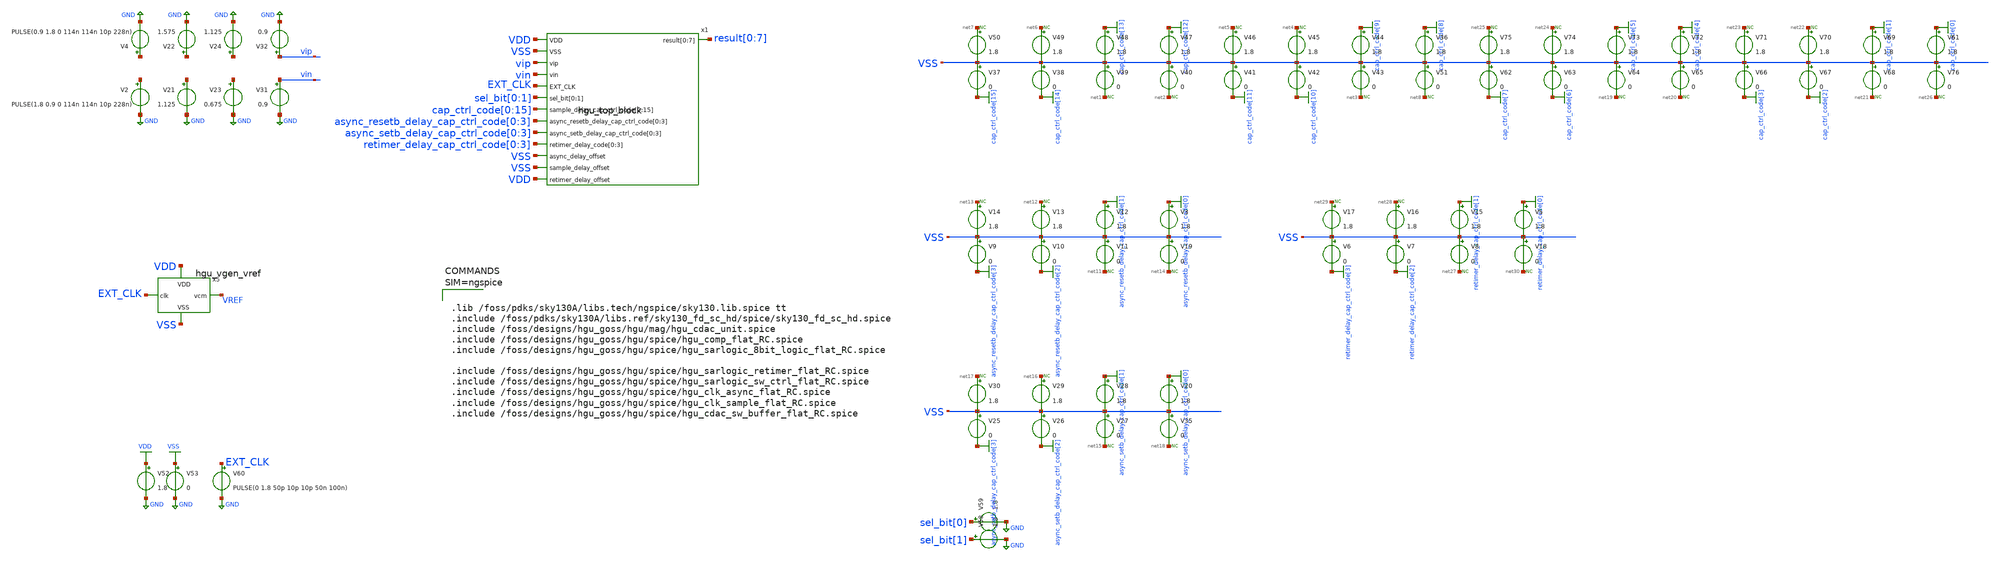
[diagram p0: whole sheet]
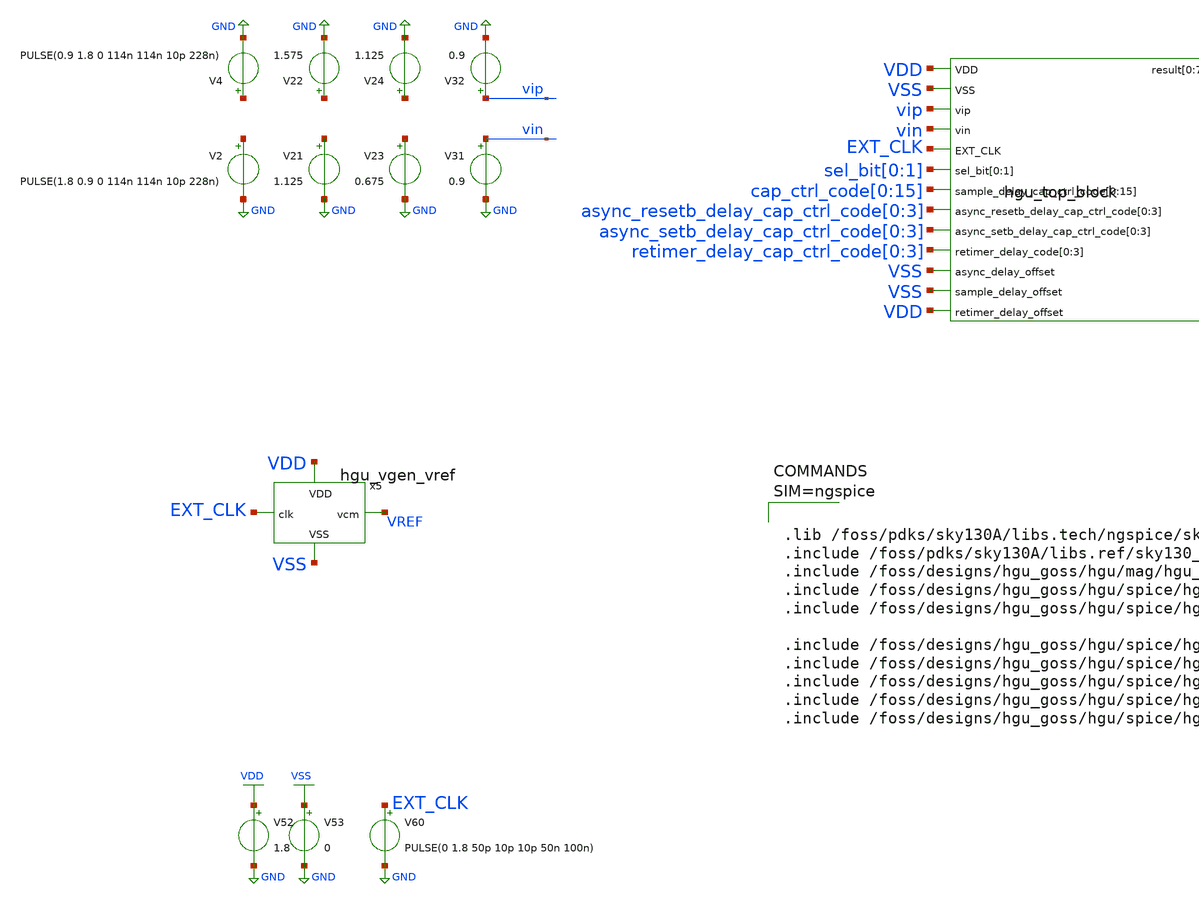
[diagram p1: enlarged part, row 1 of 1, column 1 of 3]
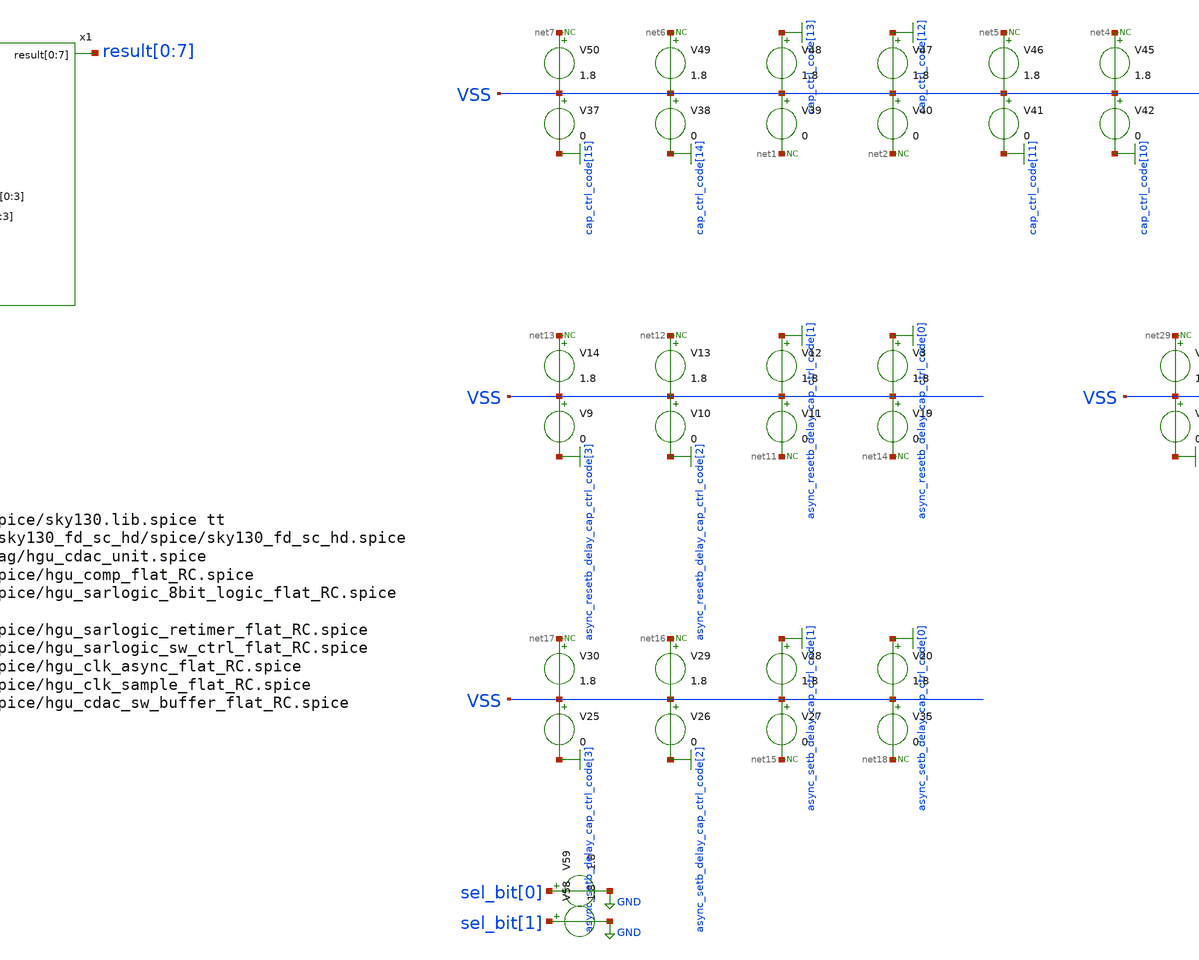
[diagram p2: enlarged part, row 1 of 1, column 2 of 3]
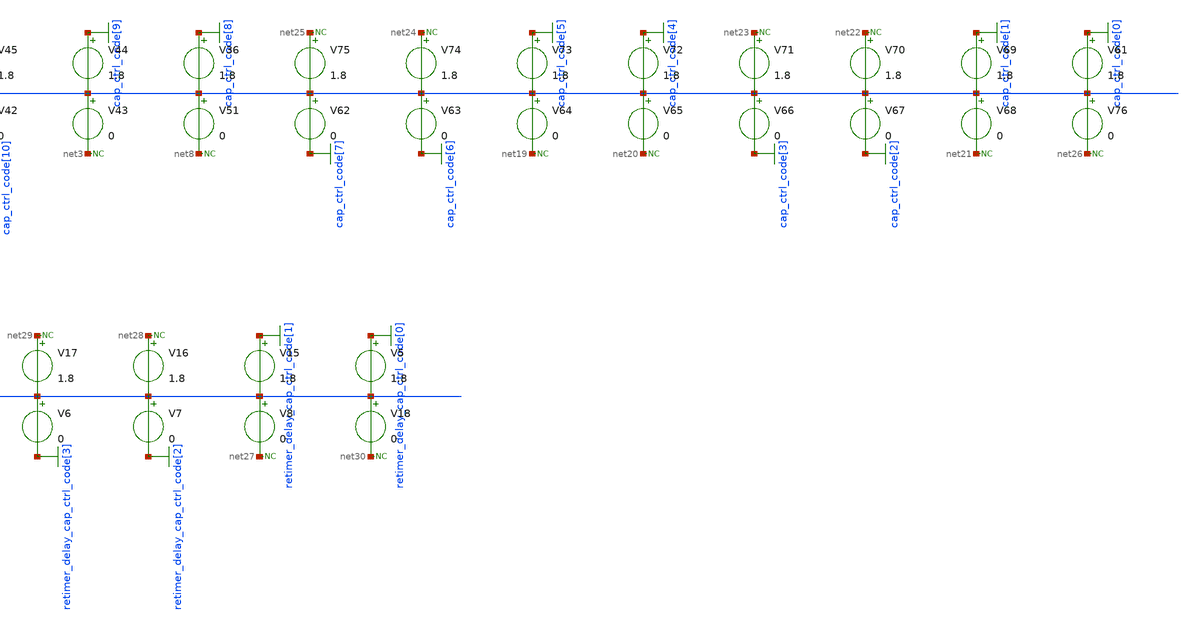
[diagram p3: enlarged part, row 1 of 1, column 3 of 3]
** sch_path: hgu/xschem/untitled-1.sch
**.subckt untitled-1
V36 cap_ctrl_code[8] VSS 1.8
V37 VSS cap_ctrl_code[15] 0
V38 VSS cap_ctrl_code[14] 0
V39 VSS net1 0
V40 VSS net2 0
V41 VSS cap_ctrl_code[11] 0
V42 VSS cap_ctrl_code[10] 0
V43 VSS net3 0
V44 cap_ctrl_code[9] VSS 1.8
V45 net4 VSS 1.8
V46 net5 VSS 1.8
V47 cap_ctrl_code[12] VSS 1.8
V48 cap_ctrl_code[13] VSS 1.8
V49 net6 VSS 1.8
V50 net7 VSS 1.8
V51 VSS net8 0
* noconn #net7
* noconn #net6
* noconn #net1
* noconn #net2
* noconn #net5
* noconn #net4
* noconn #net3
* noconn #net8
V52 VDD GND 1.8
V53 VSS GND 0
V60 EXT_CLK GND PULSE(0 1.8 50p 10p 10p 50n 100n)
V58 sel_bit[1] GND 1.8
V59 sel_bit[0] GND 1.8
V2 net9 GND PULSE(1.8 0.9 0 114n 114n 10p 228n)
V4 net10 GND PULSE(0.9 1.8 0 114n 114n 10p 228n)
V3 async_resetb_delay_cap_ctrl_code[0] VSS 1.8
V9 VSS async_resetb_delay_cap_ctrl_code[3] 0
V10 VSS async_resetb_delay_cap_ctrl_code[2] 0
V11 VSS net11 0
V12 async_resetb_delay_cap_ctrl_code[1] VSS 1.8
V13 net12 VSS 1.8
V14 net13 VSS 1.8
V19 VSS net14 0
* noconn #net13
* noconn #net12
* noconn #net11
* noconn #net14
V20 async_setb_delay_cap_ctrl_code[0] VSS 1.8
V25 VSS async_setb_delay_cap_ctrl_code[3] 0
V26 VSS async_setb_delay_cap_ctrl_code[2] 0
V27 VSS net15 0
V28 async_setb_delay_cap_ctrl_code[1] VSS 1.8
V29 net16 VSS 1.8
V30 net17 VSS 1.8
V35 VSS net18 0
* noconn #net17
* noconn #net16
* noconn #net15
* noconn #net18
V61 cap_ctrl_code[0] VSS 1.8
V62 VSS cap_ctrl_code[7] 0
V63 VSS cap_ctrl_code[6] 0
V64 VSS net19 0
V65 VSS net20 0
V66 VSS cap_ctrl_code[3] 0
V67 VSS cap_ctrl_code[2] 0
V68 VSS net21 0
V69 cap_ctrl_code[1] VSS 1.8
V70 net22 VSS 1.8
V71 net23 VSS 1.8
V72 cap_ctrl_code[4] VSS 1.8
V73 cap_ctrl_code[5] VSS 1.8
V74 net24 VSS 1.8
V75 net25 VSS 1.8
V76 VSS net26 0
* noconn #net25
* noconn #net24
* noconn #net19
* noconn #net20
* noconn #net23
* noconn #net22
* noconn #net21
* noconn #net26
V5 retimer_delay_cap_ctrl_code[0] VSS 1.8
V6 VSS retimer_delay_cap_ctrl_code[3] 0
V7 VSS retimer_delay_cap_ctrl_code[2] 0
V8 VSS net27 0
V15 retimer_delay_cap_ctrl_code[1] VSS 1.8
V16 net28 VSS 1.8
V17 net29 VSS 1.8
V18 VSS net30 0
* noconn #net29
* noconn #net28
* noconn #net27
* noconn #net30
V21 net31 GND 1.125
V22 net32 GND 1.575
V23 net33 GND 0.675
V24 net34 GND 1.125
V31 vin GND 0.9
V32 vip GND 0.9
x1 VDD result[0] result[1] result[2] result[3] result[4] result[5] result[6] result[7] VSS vip vin
+ EXT_CLK sel_bit[0] sel_bit[1] cap_ctrl_code[0] cap_ctrl_code[1] cap_ctrl_code[2] cap_ctrl_code[3]
+ cap_ctrl_code[4] cap_ctrl_code[5] cap_ctrl_code[6] cap_ctrl_code[7] cap_ctrl_code[8] cap_ctrl_code[9]
+ cap_ctrl_code[10] cap_ctrl_code[11] cap_ctrl_code[12] cap_ctrl_code[13] cap_ctrl_code[14] cap_ctrl_code[15]
+ async_resetb_delay_cap_ctrl_code[0] async_resetb_delay_cap_ctrl_code[1] async_resetb_delay_cap_ctrl_code[2]
+ async_resetb_delay_cap_ctrl_code[3] async_setb_delay_cap_ctrl_code[0] async_setb_delay_cap_ctrl_code[1]
+ async_setb_delay_cap_ctrl_code[2] async_setb_delay_cap_ctrl_code[3] retimer_delay_cap_ctrl_code[0] retimer_delay_cap_ctrl_code[1]
+ retimer_delay_cap_ctrl_code[2] retimer_delay_cap_ctrl_code[3] VSS VSS VDD hgu_top_block
x5 VDD VSS EXT_CLK VREF hgu_vgen_vref
**** begin user architecture code



.OPTIONS savecurrents
.tran 10ps 250ns

.control
	run
	plot V(sample_clk) V(vip) V(vin) V(vip)-V(vin)+0.9 V(tah_vp) V(tah_vn) V(tah_vp)-V(tah_vn)
+ V(vip)-V(vin)


.endc
.save all






.lib /foss/pdks/sky130A/libs.tech/ngspice/sky130.lib.spice tt
.include /foss/pdks/sky130A/libs.ref/sky130_fd_sc_hd/spice/sky130_fd_sc_hd.spice
.include /foss/designs/hgu_goss/hgu/mag/hgu_cdac_unit.spice
.include /foss/designs/hgu_goss/hgu/spice/hgu_comp_flat_RC.spice
.include /foss/designs/hgu_goss/hgu/spice/hgu_sarlogic_8bit_logic_flat_RC.spice

.include /foss/designs/hgu_goss/hgu/spice/hgu_sarlogic_retimer_flat_RC.spice
.include /foss/designs/hgu_goss/hgu/spice/hgu_sarlogic_sw_ctrl_flat_RC.spice
.include /foss/designs/hgu_goss/hgu/spice/hgu_clk_async_flat_RC.spice
.include /foss/designs/hgu_goss/hgu/spice/hgu_clk_sample_flat_RC.spice
.include /foss/designs/hgu_goss/hgu/spice/hgu_cdac_sw_buffer_flat_RC.spice



**** end user architecture code
**.ends
.GLOBAL GND
.GLOBAL cap_ctrl_code[15]
.GLOBAL cap_ctrl_code[14]
.GLOBAL cap_ctrl_code[13]
.GLOBAL cap_ctrl_code[12]
.GLOBAL cap_ctrl_code[11]
.GLOBAL cap_ctrl_code[10]
.GLOBAL cap_ctrl_code[9]
.GLOBAL cap_ctrl_code[8]
.GLOBAL VDD
.GLOBAL VSS
.GLOBAL async_resetb_delay_cap_ctrl_code[3]
.GLOBAL async_resetb_delay_cap_ctrl_code[2]
.GLOBAL async_resetb_delay_cap_ctrl_code[1]
.GLOBAL async_resetb_delay_cap_ctrl_code[0]
.GLOBAL async_setb_delay_cap_ctrl_code[3]
.GLOBAL async_setb_delay_cap_ctrl_code[2]
.GLOBAL async_setb_delay_cap_ctrl_code[1]
.GLOBAL async_setb_delay_cap_ctrl_code[0]
.GLOBAL cap_ctrl_code[7]
.GLOBAL cap_ctrl_code[6]
.GLOBAL cap_ctrl_code[5]
.GLOBAL cap_ctrl_code[4]
.GLOBAL cap_ctrl_code[3]
.GLOBAL cap_ctrl_code[2]
.GLOBAL cap_ctrl_code[1]
.GLOBAL cap_ctrl_code[0]
.GLOBAL retimer_delay_cap_ctrl_code[3]
.GLOBAL retimer_delay_cap_ctrl_code[2]
.GLOBAL retimer_delay_cap_ctrl_code[1]
.GLOBAL retimer_delay_cap_ctrl_code[0]
.end
